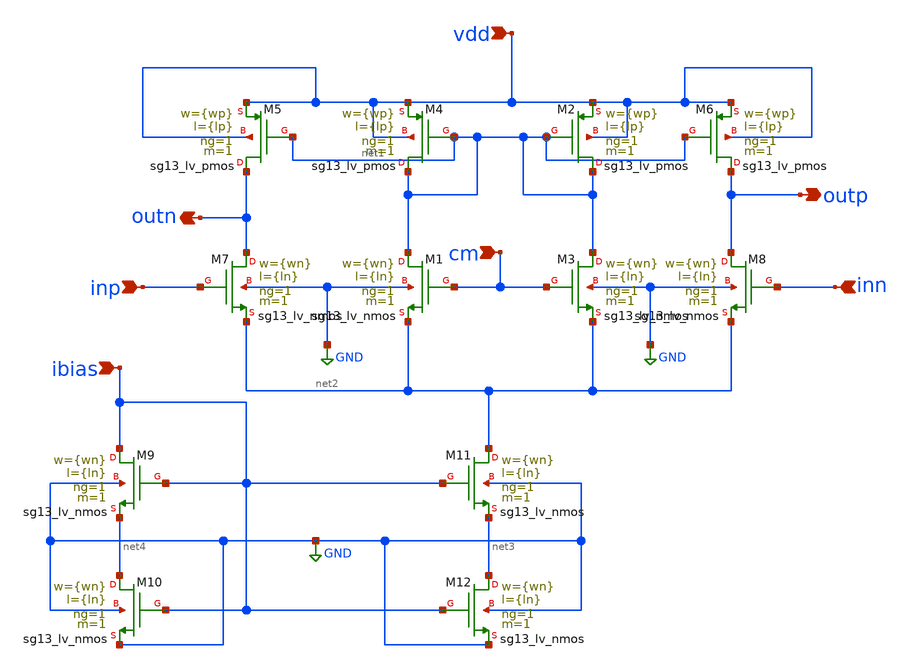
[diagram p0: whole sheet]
** sch_path: 2_Ideal_Cir/untitled.sch
**.subckt untitled inp vdd inn outp cm ibias outn
*.ipin inp
*.ipin vdd
*.ipin inn
*.opin outp
*.ipin cm
*.ipin ibias
*.opin outn
XM1 net1 cm net2 GND sg13_lv_nmos w={wn} l={ln} ng=1 m=1 mm_ok=1
XM2 net1 net1 vdd vdd sg13_lv_pmos w={wp} l={lp} ng=1 m=1 mm_ok=1
XM3 net1 cm net2 GND sg13_lv_nmos w={wn} l={ln} ng=1 m=1 mm_ok=1
XM4 net1 net1 vdd vdd sg13_lv_pmos w={wp} l={lp} ng=1 m=1 mm_ok=1
XM5 outn net1 vdd vdd sg13_lv_pmos w={wp} l={lp} ng=1 m=1 mm_ok=1
XM6 outp net1 vdd vdd sg13_lv_pmos w={wp} l={lp} ng=1 m=1 mm_ok=1
XM7 outn inp net2 GND sg13_lv_nmos w={wn} l={ln} ng=1 m=1 mm_ok=1
XM8 outp inn net2 GND sg13_lv_nmos w={wn} l={ln} ng=1 m=1 mm_ok=1
XM9 ibias ibias net4 GND sg13_lv_nmos w={wn} l={ln} ng=1 m=1 mm_ok=1
XM11 net2 ibias net3 GND sg13_lv_nmos w={wn} l={ln} ng=1 m=1 mm_ok=1
XM10 net4 ibias GND GND sg13_lv_nmos w={wn} l={ln} ng=1 m=1 mm_ok=1
XM12 net3 ibias GND GND sg13_lv_nmos w={wn} l={ln} ng=1 m=1 mm_ok=1
**.ends
.GLOBAL GND
.end
